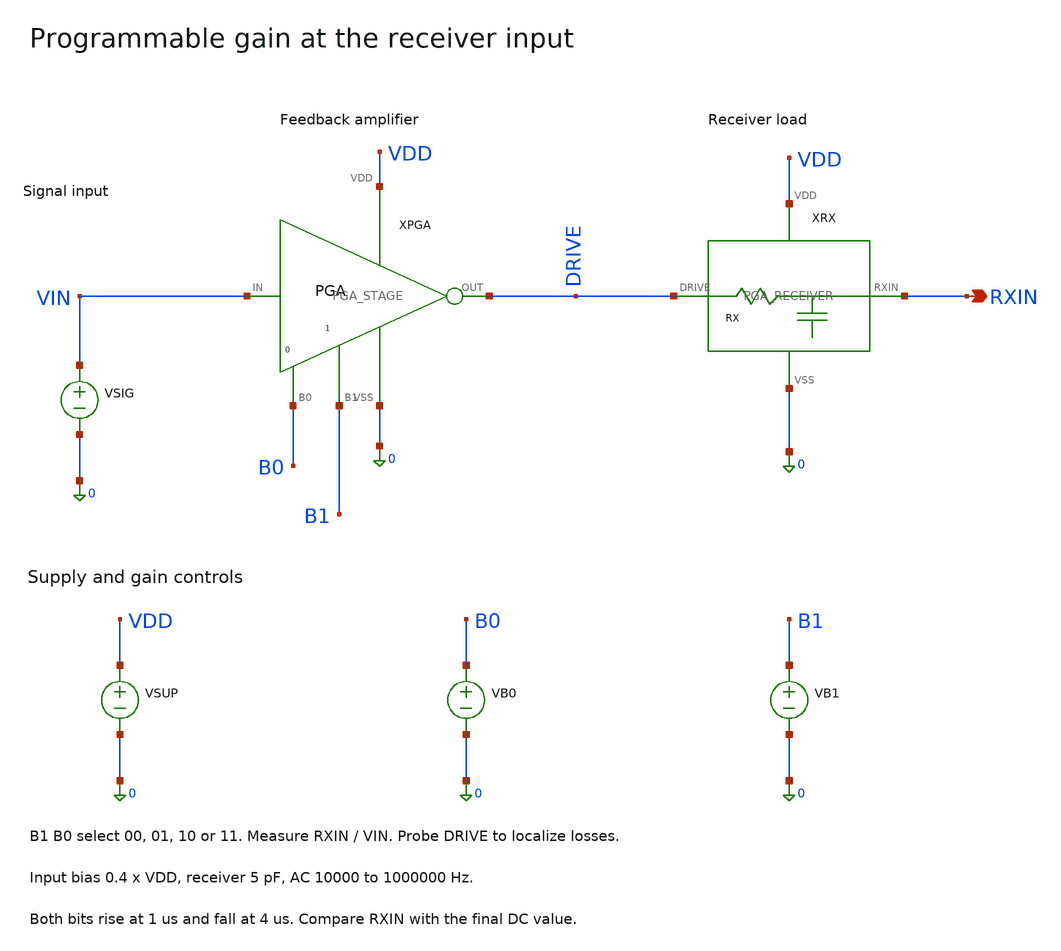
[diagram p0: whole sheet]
** sch_path: examples/sky130-programmable-gain/TB_PGA_GAIN.sch
**.subckt TB_PGA_GAIN RXIN
*.opin RXIN
XPGA VIN B0 B1 DRIVE VDD 0 PGA_STAGE
XRX DRIVE RXIN VDD 0 PGA_RECEIVER
VSIG VIN 0 DC 'VINBIAS' AC 1
VSUP VDD 0 DC 'VSUPPLY'
VB0 B0 0 DC 'VSUPPLY*BIT0' PWL(0 0 1u 0 1.002u 'VSUPPLY' 4u 'VSUPPLY' 4.002u 0 7u 0)
VB1 B1 0 DC 'VSUPPLY*BIT1' PWL(0 0 1u 0 1.002u 'VSUPPLY' 4u 'VSUPPLY' 4.002u 0 7u 0)
**.ends

* expanding   symbol:  PGA_STAGE.sym # of pins=6
** sym_path: examples/sky130-programmable-gain/PGA_STAGE.sym
** sch_path: examples/sky130-programmable-gain/PGA_STAGE.sch
.subckt PGA_STAGE IN B0 B1 OUT VDD VSS
*.ipin IN
*.opin OUT
*.iopin VDD
*.iopin VSS
*.ipin B0
*.ipin B1
RBASE SUM IN 120k m=1
R0 SUM S0 120k m=1
R1 SUM S1 60k m=1
RF OUT SUM 120k m=1
XAMP_P OUT SUM VDD VDD sky130_fd_pr__pfet_01v8 w=4.9 l=1 nf=1 ad=1.47 as=1.47 pd=10.4 ps=10.4 m=8
XAMP_N OUT SUM VSS VSS sky130_fd_pr__nfet_01v8 w=2 l=1 nf=1 ad=0.6 as=0.6 pd=4.6 ps=4.6 m=4
XSW0 IN S0 B0 VDD VSS PGA_SWITCH
XSW1 IN S1 B1 VDD VSS PGA_SWITCH
.ends


* expanding   symbol:  PGA_RECEIVER.sym # of pins=4
** sym_path: examples/sky130-programmable-gain/PGA_RECEIVER.sym
** sch_path: examples/sky130-programmable-gain/PGA_RECEIVER.sch
.subckt PGA_RECEIVER DRIVE RXIN VDD VSS
*.ipin DRIVE
*.opin RXIN
*.iopin VDD
*.iopin VSS
RISO RXIN DRIVE 2.2k m=1
CRX RXIN VSS 5p m=1
RBIAS RXIN BIAS 150k m=1
XBUF VDD RXIN MON VSS sky130_fd_pr__nfet_01v8 w=4 l=0.5 nf=1 ad=1.2 as=1.2 pd=8.6 ps=8.6 m=1
RLOAD MON VSS 56k m=1
RTOP VDD BIAS 150k m=1
RBOT BIAS VSS 100k m=1
.ends


* expanding   symbol:  PGA_SWITCH.sym # of pins=5
** sym_path: examples/sky130-programmable-gain/PGA_SWITCH.sym
** sch_path: examples/sky130-programmable-gain/PGA_SWITCH.sch
.subckt PGA_SWITCH A B EN VDD VSS
*.ipin EN
*.iopin VDD
*.iopin VSS
*.iopin A
*.iopin B
XIP ENB EN VDD VDD sky130_fd_pr__pfet_01v8 w=1.2 l=0.15 nf=1 ad=0.36 as=0.36 pd=3 ps=3 m=1
XIN ENB EN VSS VSS sky130_fd_pr__nfet_01v8 w=0.6 l=0.15 nf=1 ad=0.18 as=0.18 pd=1.8 ps=1.8 m=1
XTN B EN A VSS sky130_fd_pr__nfet_01v8 w=2 l=0.15 nf=1 ad=0.6 as=0.6 pd=4.6 ps=4.6 m=1
XTP B ENB A VDD sky130_fd_pr__pfet_01v8 w=4 l=0.15 nf=1 ad=1.2 as=1.2 pd=8.6 ps=8.6 m=1
.ends

.end
